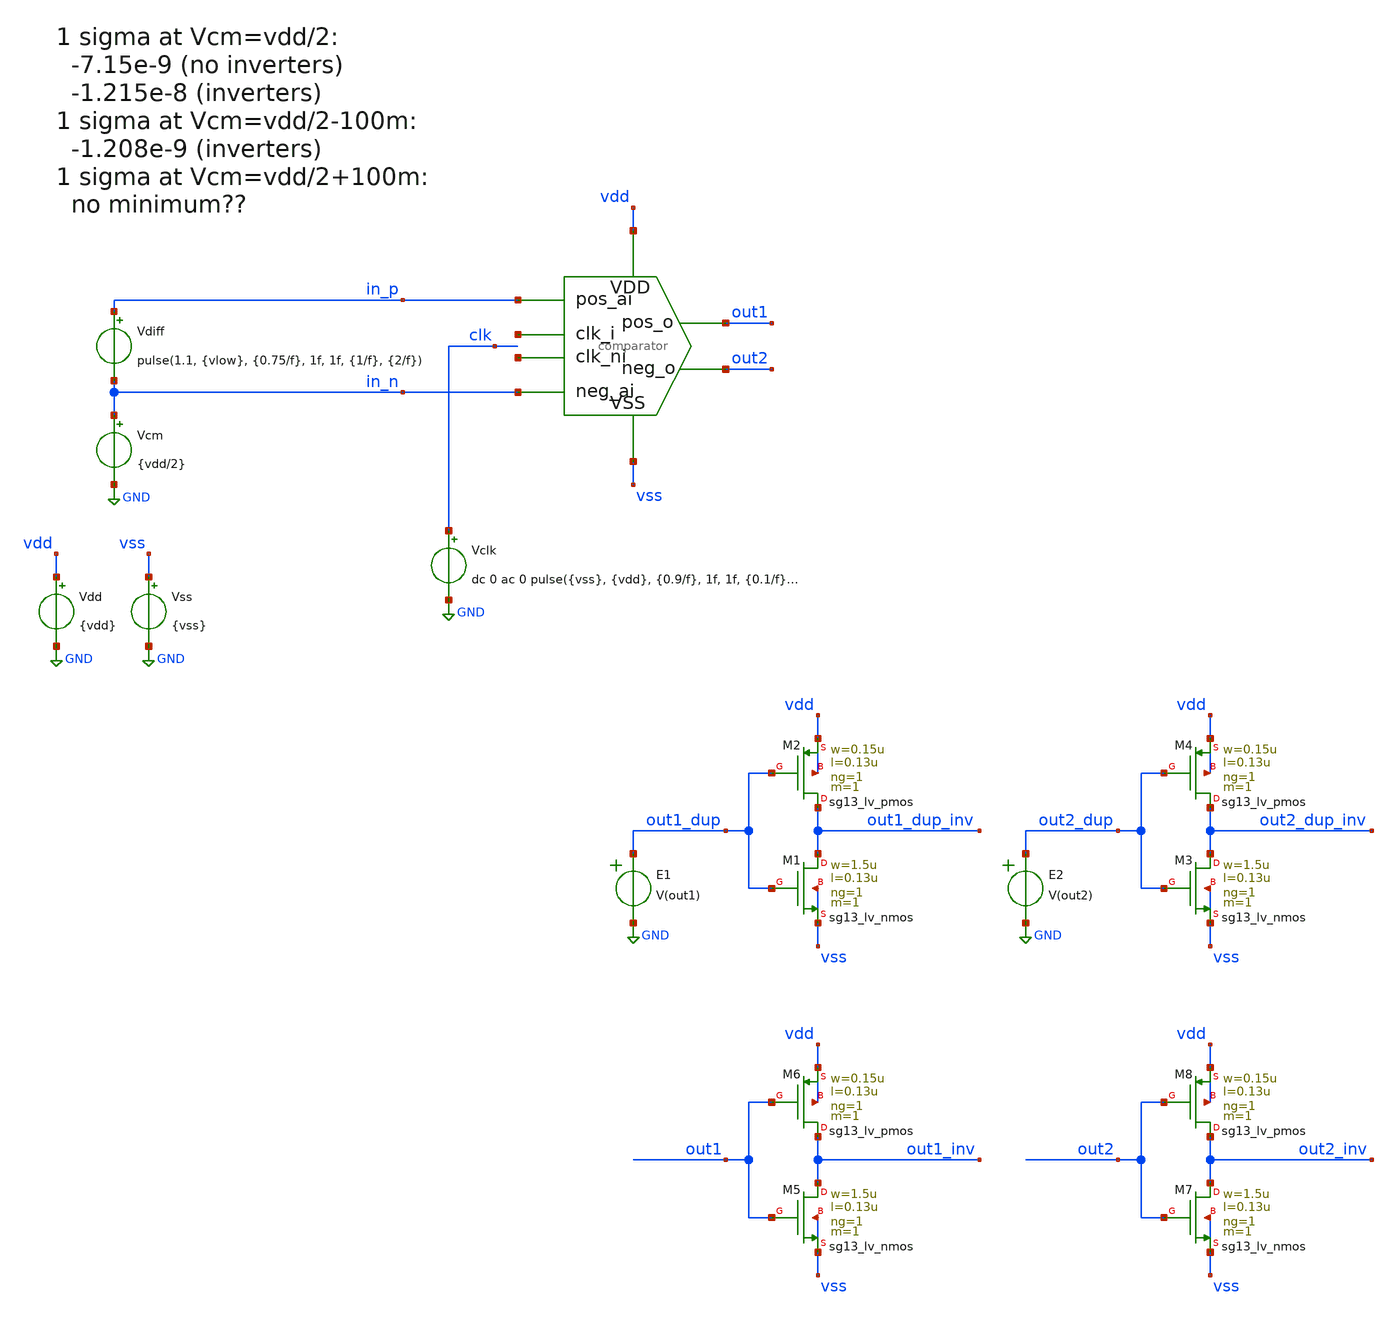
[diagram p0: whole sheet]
** sch_path: designs/comparator_sweep/comparator_tb.sch
**.subckt comparator_tb
x1 net1 in_p in_n out2 out1 vss vdd net2 comparator
Vdd vdd GND {vdd}
Vss vss GND {vss}
Vclk clk GND dc 0 ac 0 pulse({vss}, {vdd}, {0.9/f}, 1f, 1f, {0.1/f}, {1/f})
Vdiff in_p in_n pulse(1.1, {vlow}, {0.75/f}, 1f, 1f, {1/f}, {2/f})
Vcm in_n GND {vdd/2}
E1 out1_dup GND VOL=' V(out1) '
E2 out2_dup GND VOL=' V(out2) '
XM5 out1_inv out1 vss vss sg13_lv_nmos w=1.5u l=0.13u ng=1 m=1 mm_ok=1
XM6 out1_inv out1 vdd vdd sg13_lv_pmos w=0.15u l=0.13u ng=1 m=1 mm_ok=1
XM7 out2_inv out2 vss vss sg13_lv_nmos w=1.5u l=0.13u ng=1 m=1 mm_ok=1
XM8 out2_inv out2 vdd vdd sg13_lv_pmos w=0.15u l=0.13u ng=1 m=1 mm_ok=1
XM1 out1_dup_inv out1_dup vss vss sg13_lv_nmos w=1.5u l=0.13u ng=1 m=1 mm_ok=1
XM2 out1_dup_inv out1_dup vdd vdd sg13_lv_pmos w=0.15u l=0.13u ng=1 m=1 mm_ok=1
XM3 out2_dup_inv out2_dup vss vss sg13_lv_nmos w=1.5u l=0.13u ng=1 m=1 mm_ok=1
XM4 out2_dup_inv out2_dup vdd vdd sg13_lv_pmos w=0.15u l=0.13u ng=1 m=1 mm_ok=1
**** begin user architecture code

.lib $::SG13G2_MODELS/cornerMOSlv.lib mos_tt
.include $::PDK_ROOT/ihp-sg13g2/libs.ref/sg13g2_stdcell/spice/sg13g2_stdcell.spice




.param vss=0
.param vdd=1.5
.param f=100Meg

.param vlow=-4e-3

.control
save all

set wr_singlescale
set wr_vecnames
set appendwrite

compose vlow_vec values 1u 100n 10n 1n 100p 10p 1p

foreach vlow_var $&vlow_vec
  echo 'Vlow = -$vlow_var'
  alterparam vlow=-$vlow_var
  tran 0.01n 45n
  reset
  wrdata sweep.csv V(out1) V(out2)
  write comparator_tb.raw
end

.endc



**** end user architecture code
**.ends

* expanding   symbol:  comparator.sym # of pins=8
** sym_path: designs/comparator_dt/comparator.sym
** sch_path: designs/comparator_dt/comparator.sch
.subckt comparator clk_i pos_ai neg_ai neg_o pos_o VSS VDD clk_ni
*.ipin pos_ai
*.ipin neg_ai
*.ipin VSS
*.ipin VDD
*.opin neg_o
*.opin pos_o
*.ipin clk_i
*.ipin clk_ni
XM12 neg_buf clk_i VDD VDD sg13_lv_pmos w=1.0u l=0.13u ng=1 m=1 mm_ok=1
XM13 pos_buf clk_i VDD VDD sg13_lv_pmos w=1.0u l=0.13u ng=1 m=1 mm_ok=1
XM14 net1 pos_ai neg_buf VSS sg13_lv_nmos w=1.0u l=0.13u ng=1 m=1 mm_ok=1
XM15 net1 neg_ai pos_buf VSS sg13_lv_nmos w=1.0u l=0.13u ng=1 m=1 mm_ok=1
XM16 VSS clk_i net1 VSS sg13_lv_nmos w=1.0u l=0.13u ng=1 m=1 mm_ok=1
XM17 net2 clk_ni VDD VDD sg13_lv_pmos w=2.0u l=0.13u ng=2 m=1 mm_ok=1
XM18 pos_o neg_o net2 VDD sg13_lv_pmos w=2.0u l=0.13u ng=2 m=1 mm_ok=1
XM19 neg_o pos_o net2 VDD sg13_lv_pmos w=2.0u l=0.13u ng=2 m=1 mm_ok=1
XM20 VSS neg_buf pos_o VSS sg13_lv_nmos w=1.0u l=0.13u ng=1 m=1 mm_ok=1
XM21 VSS neg_o pos_o VSS sg13_lv_nmos w=1.0u l=0.13u ng=1 m=1 mm_ok=1
XM22 VSS pos_o neg_o VSS sg13_lv_nmos w=1.0u l=0.13u ng=1 m=1 mm_ok=1
XM23 VSS pos_buf neg_o VSS sg13_lv_nmos w=1.0u l=0.13u ng=1 m=1 mm_ok=1
XC1 neg_buf VSS cap_cmim w=1.41e-5 l=1.41e-5 m=1 mm_ok=1
XC2 pos_buf VSS cap_cmim w=1.41e-5 l=1.41e-5 m=1 mm_ok=1
.ends

.GLOBAL GND
.end
